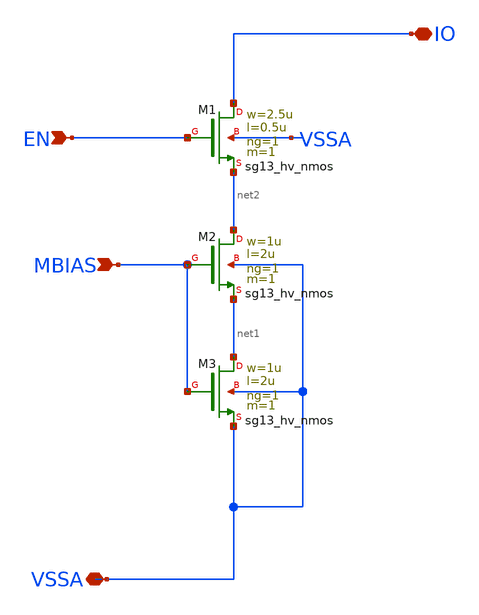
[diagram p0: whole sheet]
** sch_path: ISINK1.sch
**.subckt ISINK1 MBIAS EN IO VSSA
*.ipin MBIAS
*.ipin EN
*.iopin IO
*.iopin VSSA
XM1 IO EN net2 VSSA sg13_hv_nmos w=2.5u l=0.5u ng=1 m=1 mm_ok=1
XM2 net2 MBIAS net1 VSSA sg13_hv_nmos w=1u l=2u ng=1 m=1 mm_ok=1
XM3 net1 MBIAS VSSA VSSA sg13_hv_nmos w=1u l=2u ng=1 m=1 mm_ok=1
**.ends
.end
